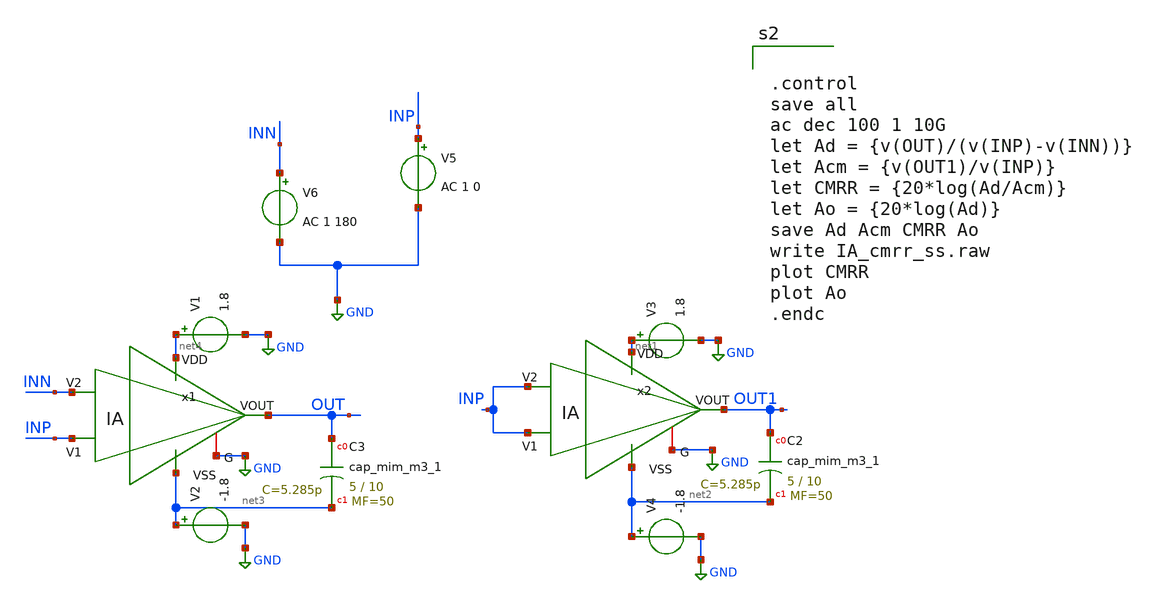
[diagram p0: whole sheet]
** sch_path: xschem/IA_cmrr_ss.sch
**.subckt IA_cmrr_ss
V6 INN GND AC 1 180
V5 INP GND AC 1 0
V1 net4 GND 1.8
V2 net3 GND -1.8
V3 net1 GND 1.8
V4 net2 GND -1.8
XC2 OUT1 net2 sky130_fd_pr__cap_mim_m3_1 W=5 L=10 MF=50 m=50
XC3 OUT net3 sky130_fd_pr__cap_mim_m3_1 W=5 L=10 MF=50 m=50
x1 net4 net3 OUT INP INN GND IA
x2 net1 net2 OUT1 INP INP GND IA
**** begin user architecture code


.control
save all
ac dec 100 1 10G
let Ad = {v(OUT)/(v(INP)-v(INN))}
let Acm = {v(OUT1)/v(INP)}
let CMRR = {20*log(Ad/Acm)}
let Ao = {20*log(Ad)}
save Ad Acm CMRR Ao
write IA_cmrr_ss.raw
plot CMRR
plot Ao
.endc



** opencircuitdesign pdks install
.lib $::SKYWATER_MODELS/sky130.lib.spice ss


**** end user architecture code
**.ends

* expanding   symbol:  /foss/designs/chipalooza2024/sky130_hcmus_ip__instramp/xschem/IA.sym # of
*+ pins=6
** sym_path: /foss/designs/chipalooza2024/sky130_hcmus_ip__instramp/xschem/IA.sym
** sch_path: /foss/designs/chipalooza2024/sky130_hcmus_ip__instramp/xschem/IA.sch
.subckt IA VDD VSS VOUT V1 V2 G
*.opin VOUT
*.iopin G
*.ipin VDD
*.ipin VSS
*.ipin V1
*.ipin V2
XR1 net9 VOUT VSS sky130_fd_pr__res_high_po W=1 L=62 mult=1 m=1
XR4 net8 net1 VSS sky130_fd_pr__res_high_po W=1 L=62 mult=1 m=1
XR6 net12 G VSS sky130_fd_pr__res_high_po W=1 L=62 mult=1 m=1
XR8 net11 net2 VSS sky130_fd_pr__res_high_po W=1 L=62 mult=1 m=1
XR9 net3 net7 VSS sky130_fd_pr__res_high_po W=1 L=62 mult=1 m=1
XR12 net10 net4 VSS sky130_fd_pr__res_high_po W=1 L=62 mult=1 m=1
XR13 net5 net6 VSS sky130_fd_pr__res_high_po W=1 L=62 mult=1 m=1
x1 VDD VSS V2 net5 net3 opamp
x2 VDD VSS V1 net6 net4 opamp
x3 VDD VSS net2 net1 VOUT opamp
XR2 net7 net5 VSS sky130_fd_pr__res_high_po W=1 L=62 mult=1 m=1
XR3 net3 net8 VSS sky130_fd_pr__res_high_po W=1 L=62 mult=1 m=1
XR5 net1 net9 VSS sky130_fd_pr__res_high_po W=1 L=62 mult=1 m=1
XR7 net6 net10 VSS sky130_fd_pr__res_high_po W=1 L=62 mult=1 m=1
XR10 net4 net11 VSS sky130_fd_pr__res_high_po W=1 L=62 mult=1 m=1
XR11 net2 net12 VSS sky130_fd_pr__res_high_po W=1 L=62 mult=1 m=1
.ends


* expanding   symbol:  /foss/designs/chipalooza2024/sky130_hcmus_ip__instramp/xschem/opamp.sym # of
*+ pins=5
** sym_path: /foss/designs/chipalooza2024/sky130_hcmus_ip__instramp/xschem/opamp.sym
** sch_path: /foss/designs/chipalooza2024/sky130_hcmus_ip__instramp/xschem/opamp.sch
.subckt opamp VDD VSS V1 V2 VOUT
*.ipin VSS
*.ipin VDD
*.ipin V2
*.ipin V1
*.opin VOUT
XM2 net5 V2 net1 VSS sky130_fd_pr__nfet_g5v0d10v5 L=1 W=18 nf=1 ad='int((nf+1)/2) * W/nf * 0.29' as='int((nf+2)/2) * W/nf * 0.29'
+ pd='2*int((nf+1)/2) * (W/nf + 0.29)' ps='2*int((nf+2)/2) * (W/nf + 0.29)' nrd='0.29 / W' nrs='0.29 / W'
+ sa=0 sb=0 sd=0 mult=1 m=1
XM1 net6 net5 VDD VDD sky130_fd_pr__pfet_g5v0d10v5 L=1 W=30 nf=1 ad='int((nf+1)/2) * W/nf * 0.29' as='int((nf+2)/2) * W/nf * 0.29'
+ pd='2*int((nf+1)/2) * (W/nf + 0.29)' ps='2*int((nf+2)/2) * (W/nf + 0.29)' nrd='0.29 / W' nrs='0.29 / W'
+ sa=0 sb=0 sd=0 mult=1 m=1
XM4 net6 V1 net1 VSS sky130_fd_pr__nfet_g5v0d10v5 L=1 W=18 nf=1 ad='int((nf+1)/2) * W/nf * 0.29' as='int((nf+2)/2) * W/nf * 0.29'
+ pd='2*int((nf+1)/2) * (W/nf + 0.29)' ps='2*int((nf+2)/2) * (W/nf + 0.29)' nrd='0.29 / W' nrs='0.29 / W'
+ sa=0 sb=0 sd=0 mult=1 m=1
XM5 net1 net4 VSS VSS sky130_fd_pr__nfet_g5v0d10v5 L=1 W=15.171 nf=1 ad='int((nf+1)/2) * W/nf * 0.29'
+ as='int((nf+2)/2) * W/nf * 0.29' pd='2*int((nf+1)/2) * (W/nf + 0.29)' ps='2*int((nf+2)/2) * (W/nf + 0.29)'
+ nrd='0.29 / W' nrs='0.29 / W' sa=0 sb=0 sd=0 mult=1 m=1
XM6 VOUT net4 VSS VSS sky130_fd_pr__nfet_g5v0d10v5 L=1 W=19 nf=1 ad='int((nf+1)/2) * W/nf * 0.29' as='int((nf+2)/2) * W/nf * 0.29'
+ pd='2*int((nf+1)/2) * (W/nf + 0.29)' ps='2*int((nf+2)/2) * (W/nf + 0.29)' nrd='0.29 / W' nrs='0.29 / W'
+ sa=0 sb=0 sd=0 mult=1 m=1
XM7 net4 net4 VSS VSS sky130_fd_pr__nfet_g5v0d10v5 L=1 W=20 nf=1 ad='int((nf+1)/2) * W/nf * 0.29' as='int((nf+2)/2) * W/nf * 0.29'
+ pd='2*int((nf+1)/2) * (W/nf + 0.29)' ps='2*int((nf+2)/2) * (W/nf + 0.29)' nrd='0.29 / W' nrs='0.29 / W'
+ sa=0 sb=0 sd=0 mult=1 m=1
XM3 net5 net5 VDD VDD sky130_fd_pr__pfet_g5v0d10v5 L=1 W=30 nf=1 ad='int((nf+1)/2) * W/nf * 0.29' as='int((nf+2)/2) * W/nf * 0.29'
+ pd='2*int((nf+1)/2) * (W/nf + 0.29)' ps='2*int((nf+2)/2) * (W/nf + 0.29)' nrd='0.29 / W' nrs='0.29 / W'
+ sa=0 sb=0 sd=0 mult=1 m=1
XM8 VOUT net6 VDD VDD sky130_fd_pr__pfet_g5v0d10v5 L=1 W=38 nf=1 ad='int((nf+1)/2) * W/nf * 0.29' as='int((nf+2)/2) * W/nf * 0.29'
+ pd='2*int((nf+1)/2) * (W/nf + 0.29)' ps='2*int((nf+2)/2) * (W/nf + 0.29)' nrd='0.29 / W' nrs='0.29 / W'
+ sa=0 sb=0 sd=0 mult=2 m=2
XR3 net2 VDD VSS sky130_fd_pr__res_high_po W=1 L=30 mult=1 m=1
XR1 net3 net2 VSS sky130_fd_pr__res_high_po W=1 L=30 mult=1 m=1
XR2 net4 net3 VSS sky130_fd_pr__res_high_po W=1 L=30 mult=1 m=1
XR4 net7 VOUT VSS sky130_fd_pr__res_high_po W=1 L=5 mult=1 m=1
XC1 net7 net6 sky130_fd_pr__cap_mim_m3_1 W=5.5 L=10 MF=10 m=10
.ends

.GLOBAL GND
.end
